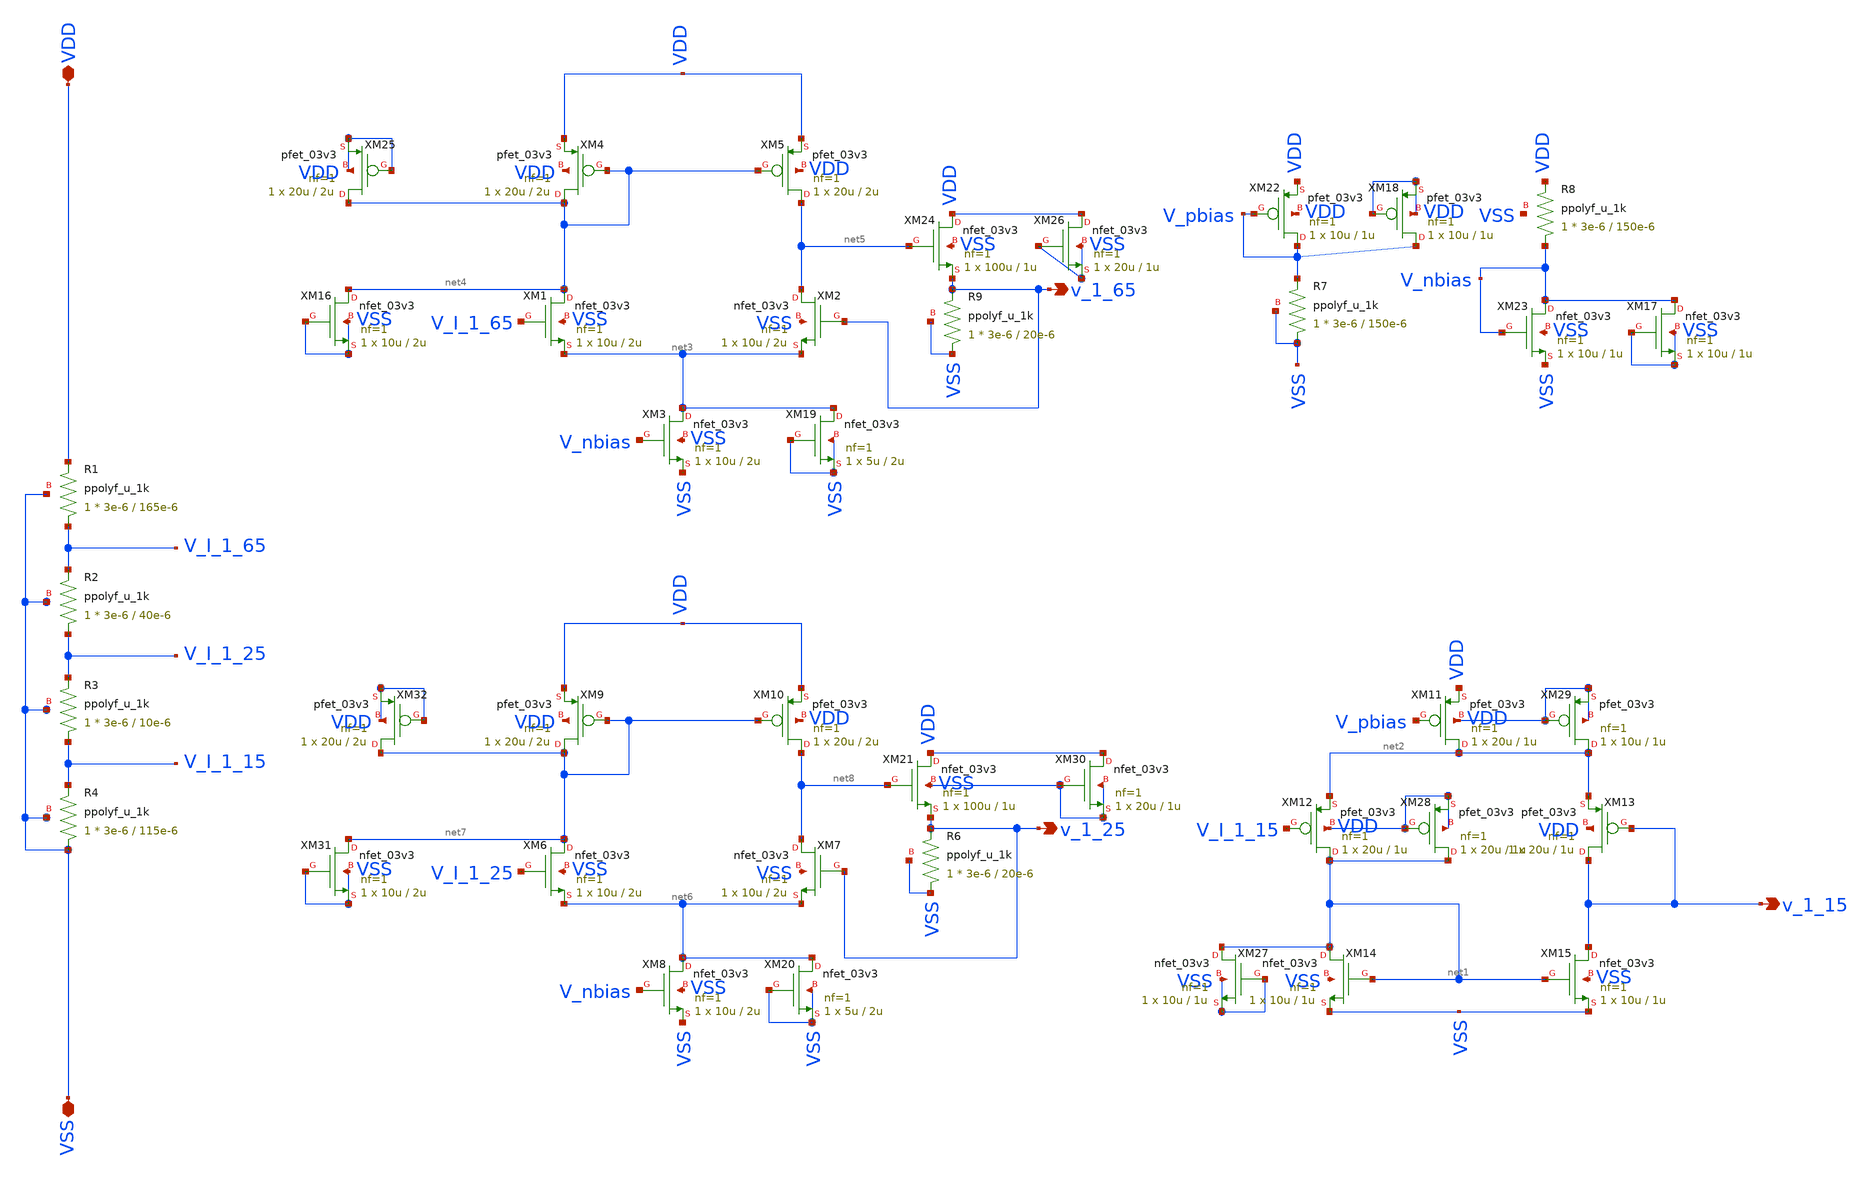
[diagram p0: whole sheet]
** sch_path: schematics/voltage_reference.sch
**.subckt voltage_reference VDD VSS v_1_65 v_1_15 v_1_25
*.iopin VDD
*.iopin VSS
*.opin v_1_65
*.opin v_1_15
*.opin v_1_25
XR1 V_I_1_65 VDD VSS ppolyf_u_1k r_width=3e-6 r_length=165e-6 m=1
XR2 V_I_1_25 V_I_1_65 VSS ppolyf_u_1k r_width=3e-6 r_length=40e-6 m=1
XR3 V_I_1_15 V_I_1_25 VSS ppolyf_u_1k r_width=3e-6 r_length=10e-6 m=1
XR4 VSS V_I_1_15 VSS ppolyf_u_1k r_width=3e-6 r_length=115e-6 m=1
XM11 net2 V_pbias VDD VDD pfet_03v3 L=1u W=20u nf=1 ad='int((nf+1)/2) * W/nf * 0.18u' as='int((nf+2)/2) * W/nf * 0.18u'
+ pd='2*int((nf+1)/2) * (W/nf + 0.18u)' ps='2*int((nf+2)/2) * (W/nf + 0.18u)' nrd='0.18u / W' nrs='0.18u / W'
+ sa=0 sb=0 sd=0 m=1
XM12 net1 V_I_1_15 net2 VDD pfet_03v3 L=1u W=20u nf=1 ad='int((nf+1)/2) * W/nf * 0.18u' as='int((nf+2)/2) * W/nf * 0.18u'
+ pd='2*int((nf+1)/2) * (W/nf + 0.18u)' ps='2*int((nf+2)/2) * (W/nf + 0.18u)' nrd='0.18u / W' nrs='0.18u / W'
+ sa=0 sb=0 sd=0 m=1
XM13 v_1_15 v_1_15 net2 VDD pfet_03v3 L=1u W=20u nf=1 ad='int((nf+1)/2) * W/nf * 0.18u' as='int((nf+2)/2) * W/nf * 0.18u'
+ pd='2*int((nf+1)/2) * (W/nf + 0.18u)' ps='2*int((nf+2)/2) * (W/nf + 0.18u)' nrd='0.18u / W' nrs='0.18u / W'
+ sa=0 sb=0 sd=0 m=1
XM14 net1 net1 VSS VSS nfet_03v3 L=1u W=10u nf=1 ad='int((nf+1)/2) * W/nf * 0.18u' as='int((nf+2)/2) * W/nf * 0.18u'
+ pd='2*int((nf+1)/2) * (W/nf + 0.18u)' ps='2*int((nf+2)/2) * (W/nf + 0.18u)' nrd='0.18u / W' nrs='0.18u / W'
+ sa=0 sb=0 sd=0 m=1
XM15 v_1_15 net1 VSS VSS nfet_03v3 L=1u W=10u nf=1 ad='int((nf+1)/2) * W/nf * 0.18u' as='int((nf+2)/2) * W/nf * 0.18u'
+ pd='2*int((nf+1)/2) * (W/nf + 0.18u)' ps='2*int((nf+2)/2) * (W/nf + 0.18u)' nrd='0.18u / W' nrs='0.18u / W'
+ sa=0 sb=0 sd=0 m=1
XM21 VDD net8 v_1_25 VSS nfet_03v3 L=1u W=100u nf=1 ad='int((nf+1)/2) * W/nf * 0.18u' as='int((nf+2)/2) * W/nf * 0.18u'
+ pd='2*int((nf+1)/2) * (W/nf + 0.18u)' ps='2*int((nf+2)/2) * (W/nf + 0.18u)' nrd='0.18u / W' nrs='0.18u / W'
+ sa=0 sb=0 sd=0 m=1
XR6 VSS v_1_25 VSS ppolyf_u_1k r_width=3e-6 r_length=20e-6 m=1
XM22 V_pbias V_pbias VDD VDD pfet_03v3 L=1u W=10u nf=1 ad='int((nf+1)/2) * W/nf * 0.18u' as='int((nf+2)/2) * W/nf * 0.18u'
+ pd='2*int((nf+1)/2) * (W/nf + 0.18u)' ps='2*int((nf+2)/2) * (W/nf + 0.18u)' nrd='0.18u / W' nrs='0.18u / W'
+ sa=0 sb=0 sd=0 m=1
XR7 VSS V_pbias VSS ppolyf_u_1k r_width=3e-6 r_length=150e-6 m=1
XM1 net4 V_I_1_65 net3 VSS nfet_03v3 L=2u W=10u nf=1 ad='int((nf+1)/2) * W/nf * 0.18u' as='int((nf+2)/2) * W/nf * 0.18u'
+ pd='2*int((nf+1)/2) * (W/nf + 0.18u)' ps='2*int((nf+2)/2) * (W/nf + 0.18u)' nrd='0.18u / W' nrs='0.18u / W'
+ sa=0 sb=0 sd=0 m=1
XM2 net5 v_1_65 net3 VSS nfet_03v3 L=2u W=10u nf=1 ad='int((nf+1)/2) * W/nf * 0.18u' as='int((nf+2)/2) * W/nf * 0.18u'
+ pd='2*int((nf+1)/2) * (W/nf + 0.18u)' ps='2*int((nf+2)/2) * (W/nf + 0.18u)' nrd='0.18u / W' nrs='0.18u / W'
+ sa=0 sb=0 sd=0 m=1
XM3 net3 V_nbias VSS VSS nfet_03v3 L=2u W=10u nf=1 ad='int((nf+1)/2) * W/nf * 0.18u' as='int((nf+2)/2) * W/nf * 0.18u'
+ pd='2*int((nf+1)/2) * (W/nf + 0.18u)' ps='2*int((nf+2)/2) * (W/nf + 0.18u)' nrd='0.18u / W' nrs='0.18u / W'
+ sa=0 sb=0 sd=0 m=1
XM4 net4 net4 VDD VDD pfet_03v3 L=2u W=20u nf=1 ad='int((nf+1)/2) * W/nf * 0.18u' as='int((nf+2)/2) * W/nf * 0.18u'
+ pd='2*int((nf+1)/2) * (W/nf + 0.18u)' ps='2*int((nf+2)/2) * (W/nf + 0.18u)' nrd='0.18u / W' nrs='0.18u / W'
+ sa=0 sb=0 sd=0 m=1
XM5 net5 net4 VDD VDD pfet_03v3 L=2u W=20u nf=1 ad='int((nf+1)/2) * W/nf * 0.18u' as='int((nf+2)/2) * W/nf * 0.18u'
+ pd='2*int((nf+1)/2) * (W/nf + 0.18u)' ps='2*int((nf+2)/2) * (W/nf + 0.18u)' nrd='0.18u / W' nrs='0.18u / W'
+ sa=0 sb=0 sd=0 m=1
XM23 V_nbias V_nbias VSS VSS nfet_03v3 L=1u W=10u nf=1 ad='int((nf+1)/2) * W/nf * 0.18u' as='int((nf+2)/2) * W/nf * 0.18u'
+ pd='2*int((nf+1)/2) * (W/nf + 0.18u)' ps='2*int((nf+2)/2) * (W/nf + 0.18u)' nrd='0.18u / W' nrs='0.18u / W'
+ sa=0 sb=0 sd=0 m=1
XR8 V_nbias VDD VSS ppolyf_u_1k r_width=3e-6 r_length=150e-6 m=1
XM6 net7 V_I_1_25 net6 VSS nfet_03v3 L=2u W=10u nf=1 ad='int((nf+1)/2) * W/nf * 0.18u' as='int((nf+2)/2) * W/nf * 0.18u'
+ pd='2*int((nf+1)/2) * (W/nf + 0.18u)' ps='2*int((nf+2)/2) * (W/nf + 0.18u)' nrd='0.18u / W' nrs='0.18u / W'
+ sa=0 sb=0 sd=0 m=1
XM7 net8 v_1_25 net6 VSS nfet_03v3 L=2u W=10u nf=1 ad='int((nf+1)/2) * W/nf * 0.18u' as='int((nf+2)/2) * W/nf * 0.18u'
+ pd='2*int((nf+1)/2) * (W/nf + 0.18u)' ps='2*int((nf+2)/2) * (W/nf + 0.18u)' nrd='0.18u / W' nrs='0.18u / W'
+ sa=0 sb=0 sd=0 m=1
XM8 net6 V_nbias VSS VSS nfet_03v3 L=2u W=10u nf=1 ad='int((nf+1)/2) * W/nf * 0.18u' as='int((nf+2)/2) * W/nf * 0.18u'
+ pd='2*int((nf+1)/2) * (W/nf + 0.18u)' ps='2*int((nf+2)/2) * (W/nf + 0.18u)' nrd='0.18u / W' nrs='0.18u / W'
+ sa=0 sb=0 sd=0 m=1
XM9 net7 net7 VDD VDD pfet_03v3 L=2u W=20u nf=1 ad='int((nf+1)/2) * W/nf * 0.18u' as='int((nf+2)/2) * W/nf * 0.18u'
+ pd='2*int((nf+1)/2) * (W/nf + 0.18u)' ps='2*int((nf+2)/2) * (W/nf + 0.18u)' nrd='0.18u / W' nrs='0.18u / W'
+ sa=0 sb=0 sd=0 m=1
XM10 net8 net7 VDD VDD pfet_03v3 L=2u W=20u nf=1 ad='int((nf+1)/2) * W/nf * 0.18u' as='int((nf+2)/2) * W/nf * 0.18u'
+ pd='2*int((nf+1)/2) * (W/nf + 0.18u)' ps='2*int((nf+2)/2) * (W/nf + 0.18u)' nrd='0.18u / W' nrs='0.18u / W'
+ sa=0 sb=0 sd=0 m=1
XM24 VDD net5 v_1_65 VSS nfet_03v3 L=1u W=100u nf=1 ad='int((nf+1)/2) * W/nf * 0.18u' as='int((nf+2)/2) * W/nf * 0.18u'
+ pd='2*int((nf+1)/2) * (W/nf + 0.18u)' ps='2*int((nf+2)/2) * (W/nf + 0.18u)' nrd='0.18u / W' nrs='0.18u / W'
+ sa=0 sb=0 sd=0 m=1
XR9 VSS v_1_65 VSS ppolyf_u_1k r_width=3e-6 r_length=20e-6 m=1
XM16 net4 VSS VSS VSS nfet_03v3 L=2u W=10u nf=1 ad='int((nf+1)/2) * W/nf * 0.18u' as='int((nf+2)/2) * W/nf * 0.18u'
+ pd='2*int((nf+1)/2) * (W/nf + 0.18u)' ps='2*int((nf+2)/2) * (W/nf + 0.18u)' nrd='0.18u / W' nrs='0.18u / W'
+ sa=0 sb=0 sd=0 m=1
XM17 V_nbias VSS VSS VSS nfet_03v3 L=1u W=10u nf=1 ad='int((nf+1)/2) * W/nf * 0.18u' as='int((nf+2)/2) * W/nf * 0.18u'
+ pd='2*int((nf+1)/2) * (W/nf + 0.18u)' ps='2*int((nf+2)/2) * (W/nf + 0.18u)' nrd='0.18u / W' nrs='0.18u / W'
+ sa=0 sb=0 sd=0 m=1
XM18 V_pbias VDD VDD VDD pfet_03v3 L=1u W=10u nf=1 ad='int((nf+1)/2) * W/nf * 0.18u' as='int((nf+2)/2) * W/nf * 0.18u'
+ pd='2*int((nf+1)/2) * (W/nf + 0.18u)' ps='2*int((nf+2)/2) * (W/nf + 0.18u)' nrd='0.18u / W' nrs='0.18u / W'
+ sa=0 sb=0 sd=0 m=1
XM19 net3 VSS VSS VSS nfet_03v3 L=2u W=5u nf=1 ad='int((nf+1)/2) * W/nf * 0.18u' as='int((nf+2)/2) * W/nf * 0.18u'
+ pd='2*int((nf+1)/2) * (W/nf + 0.18u)' ps='2*int((nf+2)/2) * (W/nf + 0.18u)' nrd='0.18u / W' nrs='0.18u / W'
+ sa=0 sb=0 sd=0 m=1
XM20 net6 VSS VSS VSS nfet_03v3 L=2u W=5u nf=1 ad='int((nf+1)/2) * W/nf * 0.18u' as='int((nf+2)/2) * W/nf * 0.18u'
+ pd='2*int((nf+1)/2) * (W/nf + 0.18u)' ps='2*int((nf+2)/2) * (W/nf + 0.18u)' nrd='0.18u / W' nrs='0.18u / W'
+ sa=0 sb=0 sd=0 m=1
XM25 net4 VDD VDD VDD pfet_03v3 L=2u W=20u nf=1 ad='int((nf+1)/2) * W/nf * 0.18u' as='int((nf+2)/2) * W/nf * 0.18u'
+ pd='2*int((nf+1)/2) * (W/nf + 0.18u)' ps='2*int((nf+2)/2) * (W/nf + 0.18u)' nrd='0.18u / W' nrs='0.18u / W'
+ sa=0 sb=0 sd=0 m=1
XM26 VDD VSS VSS VSS nfet_03v3 L=1u W=20u nf=1 ad='int((nf+1)/2) * W/nf * 0.18u' as='int((nf+2)/2) * W/nf * 0.18u'
+ pd='2*int((nf+1)/2) * (W/nf + 0.18u)' ps='2*int((nf+2)/2) * (W/nf + 0.18u)' nrd='0.18u / W' nrs='0.18u / W'
+ sa=0 sb=0 sd=0 m=1
XM27 net1 VSS VSS VSS nfet_03v3 L=1u W=10u nf=1 ad='int((nf+1)/2) * W/nf * 0.18u' as='int((nf+2)/2) * W/nf * 0.18u'
+ pd='2*int((nf+1)/2) * (W/nf + 0.18u)' ps='2*int((nf+2)/2) * (W/nf + 0.18u)' nrd='0.18u / W' nrs='0.18u / W'
+ sa=0 sb=0 sd=0 m=1
XM28 net1 VDD VDD VDD pfet_03v3 L=1u W=20u nf=1 ad='int((nf+1)/2) * W/nf * 0.18u' as='int((nf+2)/2) * W/nf * 0.18u'
+ pd='2*int((nf+1)/2) * (W/nf + 0.18u)' ps='2*int((nf+2)/2) * (W/nf + 0.18u)' nrd='0.18u / W' nrs='0.18u / W'
+ sa=0 sb=0 sd=0 m=1
XM29 net2 VDD VDD VDD pfet_03v3 L=1u W=10u nf=1 ad='int((nf+1)/2) * W/nf * 0.18u' as='int((nf+2)/2) * W/nf * 0.18u'
+ pd='2*int((nf+1)/2) * (W/nf + 0.18u)' ps='2*int((nf+2)/2) * (W/nf + 0.18u)' nrd='0.18u / W' nrs='0.18u / W'
+ sa=0 sb=0 sd=0 m=1
XM30 VDD VSS VSS VSS nfet_03v3 L=1u W=20u nf=1 ad='int((nf+1)/2) * W/nf * 0.18u' as='int((nf+2)/2) * W/nf * 0.18u'
+ pd='2*int((nf+1)/2) * (W/nf + 0.18u)' ps='2*int((nf+2)/2) * (W/nf + 0.18u)' nrd='0.18u / W' nrs='0.18u / W'
+ sa=0 sb=0 sd=0 m=1
XM31 net7 VSS VSS VSS nfet_03v3 L=2u W=10u nf=1 ad='int((nf+1)/2) * W/nf * 0.18u' as='int((nf+2)/2) * W/nf * 0.18u'
+ pd='2*int((nf+1)/2) * (W/nf + 0.18u)' ps='2*int((nf+2)/2) * (W/nf + 0.18u)' nrd='0.18u / W' nrs='0.18u / W'
+ sa=0 sb=0 sd=0 m=1
XM32 net7 VDD VDD VDD pfet_03v3 L=2u W=20u nf=1 ad='int((nf+1)/2) * W/nf * 0.18u' as='int((nf+2)/2) * W/nf * 0.18u'
+ pd='2*int((nf+1)/2) * (W/nf + 0.18u)' ps='2*int((nf+2)/2) * (W/nf + 0.18u)' nrd='0.18u / W' nrs='0.18u / W'
+ sa=0 sb=0 sd=0 m=1
**.ends
.end
